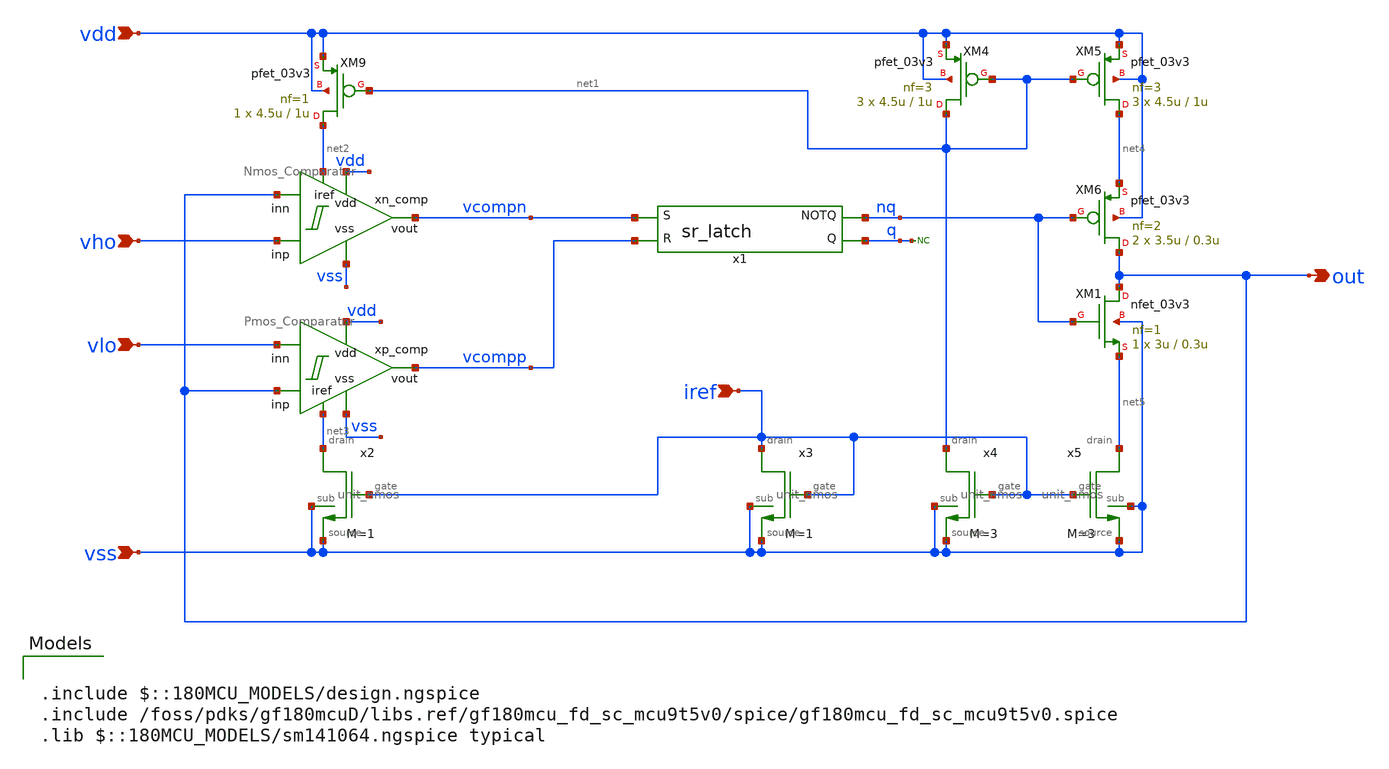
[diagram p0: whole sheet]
** sch_path: designs/libs/core_analog/oscillator/triangle_osc.sch
**.subckt triangle_osc iref vss vho vlo out vdd
*.ipin iref
*.ipin vss
*.ipin vho
*.ipin vlo
*.opin out
*.ipin vdd
XM4 net1 net1 vdd vdd pfet_03v3 L=1u W=4.5u nf=3 ad='int((nf+1)/2) * W/nf * 0.18u' as='int((nf+2)/2) * W/nf * 0.18u'
+ pd='2*int((nf+1)/2) * (W/nf + 0.18u)' ps='2*int((nf+2)/2) * (W/nf + 0.18u)' nrd='0.18u / W' nrs='0.18u / W'
+ sa=0 sb=0 sd=0 m=3
XM5 net4 net1 vdd vdd pfet_03v3 L=1u W=4.5u nf=3 ad='int((nf+1)/2) * W/nf * 0.18u' as='int((nf+2)/2) * W/nf * 0.18u'
+ pd='2*int((nf+1)/2) * (W/nf + 0.18u)' ps='2*int((nf+2)/2) * (W/nf + 0.18u)' nrd='0.18u / W' nrs='0.18u / W'
+ sa=0 sb=0 sd=0 m=3
XM6 out nq net4 vdd pfet_03v3 L=0.3u W=3.5u nf=2 ad='int((nf+1)/2) * W/nf * 0.18u' as='int((nf+2)/2) * W/nf * 0.18u'
+ pd='2*int((nf+1)/2) * (W/nf + 0.18u)' ps='2*int((nf+2)/2) * (W/nf + 0.18u)' nrd='0.18u / W' nrs='0.18u / W'
+ sa=0 sb=0 sd=0 m=2
XM9 net2 net1 vdd vdd pfet_03v3 L=1u W=4.5u nf=1 ad='int((nf+1)/2) * W/nf * 0.18u' as='int((nf+2)/2) * W/nf * 0.18u'
+ pd='2*int((nf+1)/2) * (W/nf + 0.18u)' ps='2*int((nf+2)/2) * (W/nf + 0.18u)' nrd='0.18u / W' nrs='0.18u / W'
+ sa=0 sb=0 sd=0 m=1
xn_comp vdd vcompn vho vss out net2 Nmos_Comparator
xp_comp vdd vcompp out vss vlo net3 Pmos_Comparator
x1 vcompp q nq vcompn sr_latch
x3 iref vss iref vss unit_nmos M=1
x4 net1 vss iref vss unit_nmos M=3
x5 net5 vss iref vss unit_nmos M=3
x2 net3 vss iref vss unit_nmos M=1
* noconn q
XM1 out nq net5 vss nfet_03v3 L=0.3u W=3u nf=1 ad='int((nf+1)/2) * W/nf * 0.18u' as='int((nf+2)/2) * W/nf * 0.18u'
+ pd='2*int((nf+1)/2) * (W/nf + 0.18u)' ps='2*int((nf+2)/2) * (W/nf + 0.18u)' nrd='0.18u / W' nrs='0.18u / W'
+ sa=0 sb=0 sd=0 m=1
**** begin user architecture code

.include $::180MCU_MODELS/design.ngspice
.include /foss/pdks/gf180mcuD/libs.ref/gf180mcu_fd_sc_mcu9t5v0/spice/gf180mcu_fd_sc_mcu9t5v0.spice
.lib $::180MCU_MODELS/sm141064.ngspice typical

**** end user architecture code
**.ends

* expanding   symbol:  libs/core_analog/Comparator/Nmos_Comparator.sym # of pins=6
** sym_path: designs/libs/core_analog/Comparator/Nmos_Comparator.sym
** sch_path: designs/libs/core_analog/Comparator/Nmos_Comparator.sch
.subckt Nmos_Comparator vdd vout inp vss inn iref
*.ipin vss
*.ipin vdd
*.ipin iref
*.ipin inn
*.ipin inp
*.opin vout
XM3 net1 net1 vss vss nfet_03v3 L=1u W=3.5u nf=1 ad='int((nf+1)/2) * W/nf * 0.18u' as='int((nf+2)/2) * W/nf * 0.18u'
+ pd='2*int((nf+1)/2) * (W/nf + 0.18u)' ps='2*int((nf+2)/2) * (W/nf + 0.18u)' nrd='0.18u / W' nrs='0.18u / W'
+ sa=0 sb=0 sd=0 m=1
XM4 vout net1 vss vss nfet_03v3 L=1u W=3.5u nf=1 ad='int((nf+1)/2) * W/nf * 0.18u' as='int((nf+2)/2) * W/nf * 0.18u'
+ pd='2*int((nf+1)/2) * (W/nf + 0.18u)' ps='2*int((nf+2)/2) * (W/nf + 0.18u)' nrd='0.18u / W' nrs='0.18u / W'
+ sa=0 sb=0 sd=0 m=1
XM5 net2 inn net3 vss nfet_03v3 L=1u W=4u nf=1 ad='int((nf+1)/2) * W/nf * 0.18u' as='int((nf+2)/2) * W/nf * 0.18u'
+ pd='2*int((nf+1)/2) * (W/nf + 0.18u)' ps='2*int((nf+2)/2) * (W/nf + 0.18u)' nrd='0.18u / W' nrs='0.18u / W'
+ sa=0 sb=0 sd=0 m=1
XM6 net4 inp net3 vss nfet_03v3 L=1u W=4u nf=1 ad='int((nf+1)/2) * W/nf * 0.18u' as='int((nf+2)/2) * W/nf * 0.18u'
+ pd='2*int((nf+1)/2) * (W/nf + 0.18u)' ps='2*int((nf+2)/2) * (W/nf + 0.18u)' nrd='0.18u / W' nrs='0.18u / W'
+ sa=0 sb=0 sd=0 m=1
XM7 net1 net2 vdd vdd pfet_03v3 L=0.5u W=16.5u nf=4 ad='int((nf+1)/2) * W/nf * 0.18u' as='int((nf+2)/2) * W/nf * 0.18u'
+ pd='2*int((nf+1)/2) * (W/nf + 0.18u)' ps='2*int((nf+2)/2) * (W/nf + 0.18u)' nrd='0.18u / W' nrs='0.18u / W'
+ sa=0 sb=0 sd=0 m=1
XM9 net4 net4 vdd vdd pfet_03v3 L=0.5u W=10u nf=2 ad='int((nf+1)/2) * W/nf * 0.18u' as='int((nf+2)/2) * W/nf * 0.18u'
+ pd='2*int((nf+1)/2) * (W/nf + 0.18u)' ps='2*int((nf+2)/2) * (W/nf + 0.18u)' nrd='0.18u / W' nrs='0.18u / W'
+ sa=0 sb=0 sd=0 m=1
XM11 net2 net2 vdd vdd pfet_03v3 L=0.5u W=10u nf=2 ad='int((nf+1)/2) * W/nf * 0.18u' as='int((nf+2)/2) * W/nf * 0.18u'
+ pd='2*int((nf+1)/2) * (W/nf + 0.18u)' ps='2*int((nf+2)/2) * (W/nf + 0.18u)' nrd='0.18u / W' nrs='0.18u / W'
+ sa=0 sb=0 sd=0 m=1
XM12 vout net4 vdd vdd pfet_03v3 L=0.5u W=16.5u nf=4 ad='int((nf+1)/2) * W/nf * 0.18u' as='int((nf+2)/2) * W/nf * 0.18u'
+ pd='2*int((nf+1)/2) * (W/nf + 0.18u)' ps='2*int((nf+2)/2) * (W/nf + 0.18u)' nrd='0.18u / W' nrs='0.18u / W'
+ sa=0 sb=0 sd=0 m=1
XM1 net4 net2 vdd vdd pfet_03v3 L=0.5u W=10u nf=2 ad='int((nf+1)/2) * W/nf * 0.18u' as='int((nf+2)/2) * W/nf * 0.18u'
+ pd='2*int((nf+1)/2) * (W/nf + 0.18u)' ps='2*int((nf+2)/2) * (W/nf + 0.18u)' nrd='0.18u / W' nrs='0.18u / W'
+ sa=0 sb=0 sd=0 m=1
XM2 net2 net4 vdd vdd pfet_03v3 L=0.5u W=10u nf=2 ad='int((nf+1)/2) * W/nf * 0.18u' as='int((nf+2)/2) * W/nf * 0.18u'
+ pd='2*int((nf+1)/2) * (W/nf + 0.18u)' ps='2*int((nf+2)/2) * (W/nf + 0.18u)' nrd='0.18u / W' nrs='0.18u / W'
+ sa=0 sb=0 sd=0 m=1
XM8 iref iref vss vss nfet_03v3 L=1u W=2.5u nf=1 ad='int((nf+1)/2) * W/nf * 0.18u' as='int((nf+2)/2) * W/nf * 0.18u'
+ pd='2*int((nf+1)/2) * (W/nf + 0.18u)' ps='2*int((nf+2)/2) * (W/nf + 0.18u)' nrd='0.18u / W' nrs='0.18u / W'
+ sa=0 sb=0 sd=0 m=1
XM10 net3 iref vss vss nfet_03v3 L=1u W=5u nf=2 ad='int((nf+1)/2) * W/nf * 0.18u' as='int((nf+2)/2) * W/nf * 0.18u'
+ pd='2*int((nf+1)/2) * (W/nf + 0.18u)' ps='2*int((nf+2)/2) * (W/nf + 0.18u)' nrd='0.18u / W' nrs='0.18u / W'
+ sa=0 sb=0 sd=0 m=1
.ends


* expanding   symbol:  libs/core_analog/oscillator/sr_latch.sym # of pins=4
** sym_path: designs/libs/core_analog/oscillator/sr_latch.sym
** sch_path: designs/libs/core_analog/oscillator/sr_latch.sch
.subckt sr_latch R Q NOTQ S
*.ipin R
*.ipin S
*.opin Q
*.opin NOTQ
x1 R NOTQ VSSd VDDd VSSd VDDd Q gf180mcu_fd_sc_mcu9t5v0__nor2_2
x2 Q S VSSd VDDd VSSd VDDd NOTQ gf180mcu_fd_sc_mcu9t5v0__nor2_2
**** begin user architecture code

.include $::180MCU_MODELS/design.ngspice
.include /foss/pdks/gf180mcuD/libs.ref/gf180mcu_fd_sc_mcu9t5v0/spice/gf180mcu_fd_sc_mcu9t5v0.spice
.lib $::180MCU_MODELS/sm141064.ngspice typical

**** end user architecture code
.ends


* expanding   symbol:  libs/core_analog/unit_nmos/unit_nmos.sym # of pins=4
** sym_path: libs/core_analog/unit_nmos/unit_nmos.sym
** sch_path: libs/core_analog/unit_nmos/unit_nmos.sch
.subckt unit_nmos drain sub gate source
*.iopin drain
*.iopin source
*.iopin sub
*.iopin gate
XM1 drain gate source sub nfet_03v3 L=1u W=2.5u nf=1 ad='int((nf+1)/2) * W/nf * 0.18u' as='int((nf+2)/2) * W/nf * 0.18u'
+ pd='2*int((nf+1)/2) * (W/nf + 0.18u)' ps='2*int((nf+2)/2) * (W/nf + 0.18u)' nrd='0.18u / W' nrs='0.18u / W'
+ sa=0 sb=0 sd=0 m={M}
**** begin user architecture code

.param M=1

**** end user architecture code
.ends

.end
